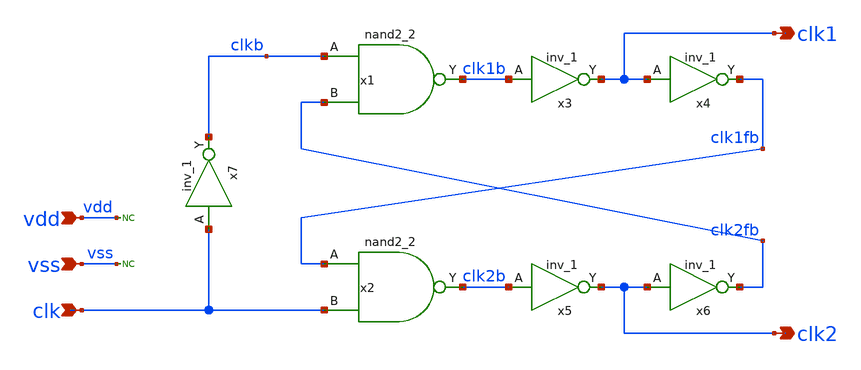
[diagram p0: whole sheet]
** sch_path: pll/pll_nol_clkb/xschem/pll_nol_clkb.sch
**.subckt pll_nol_clkb clk1 clk2 vdd vss clk
*.opin clk1
*.opin clk2
*.ipin vdd
*.ipin vss
*.ipin clk
x3 clk1b vss vss vdd vdd clk1 sky130_fd_sc_hd__inv_1
x4 clk1 vss vss vdd vdd clk1fb sky130_fd_sc_hd__inv_1
x5 clk2b vss vss vdd vdd clk2 sky130_fd_sc_hd__inv_1
x6 clk2 vss vss vdd vdd clk2fb sky130_fd_sc_hd__inv_1
x7 clk vss vss vdd vdd clkb sky130_fd_sc_hd__inv_1
x1 clkb clk2fb vss vss vdd vdd clk1b sky130_fd_sc_hd__nand2_2
x2 clk1fb clk vss vss vdd vdd clk2b sky130_fd_sc_hd__nand2_2
* noconn vdd
* noconn vss
**** begin user architecture code

.options wnflag=1
.include $::SKYWATER_MODELS/cells/nfet_01v8/sky130_fd_pr__nfet_01v8__tt.corner.spice
.include $::SKYWATER_MODELS/cells/nfet_01v8_lvt/sky130_fd_pr__nfet_01v8_lvt__tt.corner.spice
.include $::SKYWATER_MODELS/cells/pfet_01v8/sky130_fd_pr__pfet_01v8__tt.corner.spice
.include $::SKYWATER_MODELS/cells/nfet_03v3_nvt/sky130_fd_pr__nfet_03v3_nvt__tt.corner.spice
.include $::SKYWATER_MODELS/cells/nfet_05v0_nvt/sky130_fd_pr__nfet_05v0_nvt__tt.corner.spice
.include $::SKYWATER_MODELS/cells/esd_nfet_01v8/sky130_fd_pr__esd_nfet_01v8__tt.corner.spice
.include $::SKYWATER_MODELS/cells/pfet_01v8_lvt/sky130_fd_pr__pfet_01v8_lvt__tt.corner.spice
.include $::SKYWATER_MODELS/cells/pfet_01v8_hvt/sky130_fd_pr__pfet_01v8_hvt__tt.corner.spice
.include $::SKYWATER_MODELS/cells/esd_pfet_g5v0d10v5/sky130_fd_pr__esd_pfet_g5v0d10v5__tt.corner.spice
.include $::SKYWATER_MODELS/cells/pfet_g5v0d10v5/sky130_fd_pr__pfet_g5v0d10v5__tt.corner.spice
.include $::SKYWATER_MODELS/cells/pfet_g5v0d16v0/sky130_fd_pr__pfet_g5v0d16v0__tt.corner.spice
.include $::SKYWATER_MODELS/cells/nfet_g5v0d10v5/sky130_fd_pr__nfet_g5v0d10v5__tt.corner.spice
.include $::SKYWATER_MODELS/cells/nfet_g5v0d16v0/sky130_fd_pr__nfet_g5v0d16v0__tt_discrete.corner.spice
.include $::SKYWATER_MODELS/cells/esd_nfet_g5v0d10v5/sky130_fd_pr__esd_nfet_g5v0d10v5__tt.corner.spice
.include $::SKYWATER_MODELS/models/corners/tt/nonfet.spice

.include $::SKYWATER_MODELS/cells/cap_var_hvt/sky130_fd_pr__cap_var_hvt.model.spice

* Mismatch parameters
.include $::SKYWATER_MODELS/cells/nfet_01v8/sky130_fd_pr__nfet_01v8__mismatch.corner.spice
.include $::SKYWATER_MODELS/cells/pfet_01v8/sky130_fd_pr__pfet_01v8__mismatch.corner.spice
.include $::SKYWATER_MODELS/cells/nfet_01v8_lvt/sky130_fd_pr__nfet_01v8_lvt__mismatch.corner.spice
.include $::SKYWATER_MODELS/cells/pfet_01v8_lvt/sky130_fd_pr__pfet_01v8_lvt__mismatch.corner.spice
.include $::SKYWATER_MODELS/cells/pfet_01v8_hvt/sky130_fd_pr__pfet_01v8_hvt__mismatch.corner.spice
.include $::SKYWATER_MODELS/cells/nfet_g5v0d10v5/sky130_fd_pr__nfet_g5v0d10v5__mismatch.corner.spice
.include $::SKYWATER_MODELS/cells/pfet_g5v0d10v5/sky130_fd_pr__pfet_g5v0d10v5__mismatch.corner.spice
.include $::SKYWATER_MODELS/cells/nfet_05v0_nvt/sky130_fd_pr__nfet_05v0_nvt__mismatch.corner.spice
.include $::SKYWATER_MODELS/cells/nfet_03v3_nvt/sky130_fd_pr__nfet_03v3_nvt__mismatch.corner.spice

* Resistor$::SKYWATER_MODELS/Capacitor
.include $::SKYWATER_MODELS/models/r+c/res_typical__cap_typical.spice
.include $::SKYWATER_MODELS/models/r+c/res_typical__cap_typical__lin.spice

* Special cells
.include $::SKYWATER_MODELS/models/corners/tt/specialized_cells.spice

* All models
.include $::SKYWATER_MODELS/models/all.spice

* Corner
.include $::SKYWATER_MODELS/models/corners/tt/rf.spice

* .include $::SKYWATER_STDCELLS/cells/
.include $::SKYWATER_STDCELLS/cells/and2/sky130_fd_sc_hd__and2_1.spice
.include $::SKYWATER_STDCELLS/cells/and2/sky130_fd_sc_hd__and2_2.spice
.include $::SKYWATER_STDCELLS_HS/cells/and2/sky130_fd_sc_hs__and2_1.spice
.include $::SKYWATER_STDCELLS_HS/cells/and2/sky130_fd_sc_hs__and2_2.spice

.include $::SKYWATER_STDCELLS/cells/nand2/sky130_fd_sc_hd__nand2_1.spice
.include $::SKYWATER_STDCELLS/cells/nand2/sky130_fd_sc_hd__nand2_2.spice
.include $::SKYWATER_STDCELLS_HS/cells/nand2/sky130_fd_sc_hs__nand2_1.spice
.include $::SKYWATER_STDCELLS_HS/cells/nand2/sky130_fd_sc_hs__nand2_2.spice

.include $::SKYWATER_STDCELLS/cells/or2/sky130_fd_sc_hd__or2_1.spice
.include $::SKYWATER_STDCELLS/cells/or2/sky130_fd_sc_hd__or2_2.spice
.include $::SKYWATER_STDCELLS_HS/cells/or2/sky130_fd_sc_hs__or2_1.spice
.include $::SKYWATER_STDCELLS_HS/cells/or2/sky130_fd_sc_hs__or2_2.spice

.include $::SKYWATER_STDCELLS/cells/buf/sky130_fd_sc_hd__buf_1.spice
.include $::SKYWATER_STDCELLS_HS/cells/buf/sky130_fd_sc_hs__buf_1.spice

.include $::SKYWATER_STDCELLS/cells/dfrbp/sky130_fd_sc_hd__dfrbp_1.spice
.include $::SKYWATER_STDCELLS/cells/dfrbp/sky130_fd_sc_hd__dfrbp_2.spice
.include $::SKYWATER_STDCELLS_HS/cells/dfrbp/sky130_fd_sc_hs__dfrbp_1.spice
.include $::SKYWATER_STDCELLS_HS/cells/dfrbp/sky130_fd_sc_hs__dfrbp_2.spice

.include $::SKYWATER_STDCELLS/cells/inv/sky130_fd_sc_hd__inv_1.spice
.include $::SKYWATER_STDCELLS/cells/inv/sky130_fd_sc_hd__inv_2.spice
.include $::SKYWATER_STDCELLS/cells/inv/sky130_fd_sc_hd__inv_4.spice
.include $::SKYWATER_STDCELLS/cells/inv/sky130_fd_sc_hd__inv_8.spice
.include $::SKYWATER_STDCELLS/cells/inv/sky130_fd_sc_hd__inv_16.spice
.include $::SKYWATER_STDCELLS_HS/cells/inv/sky130_fd_sc_hs__inv_1.spice
.include $::SKYWATER_STDCELLS_HS/cells/inv/sky130_fd_sc_hs__inv_2.spice
.include $::SKYWATER_STDCELLS_HS/cells/inv/sky130_fd_sc_hs__inv_4.spice
.include $::SKYWATER_STDCELLS_HS/cells/inv/sky130_fd_sc_hs__inv_8.spice
.include $::SKYWATER_STDCELLS_HS/cells/inv/sky130_fd_sc_hs__inv_16.spice

.include $::SKYWATER_STDCELLS/cells/mux2/sky130_fd_sc_hd__mux2_2.spice
.include $::SKYWATER_STDCELLS/cells/nand2/sky130_fd_sc_hd__nand2_1.spice

.include $::SKYWATER_STDCELLS/cells/tap/sky130_fd_sc_hd__tap_2.spice
.include $::SKYWATER_STDCELLS/cells/tapvpwrvgnd/sky130_fd_sc_hd__tapvpwrvgnd_1.spice

**** end user architecture code
**.ends
.end
